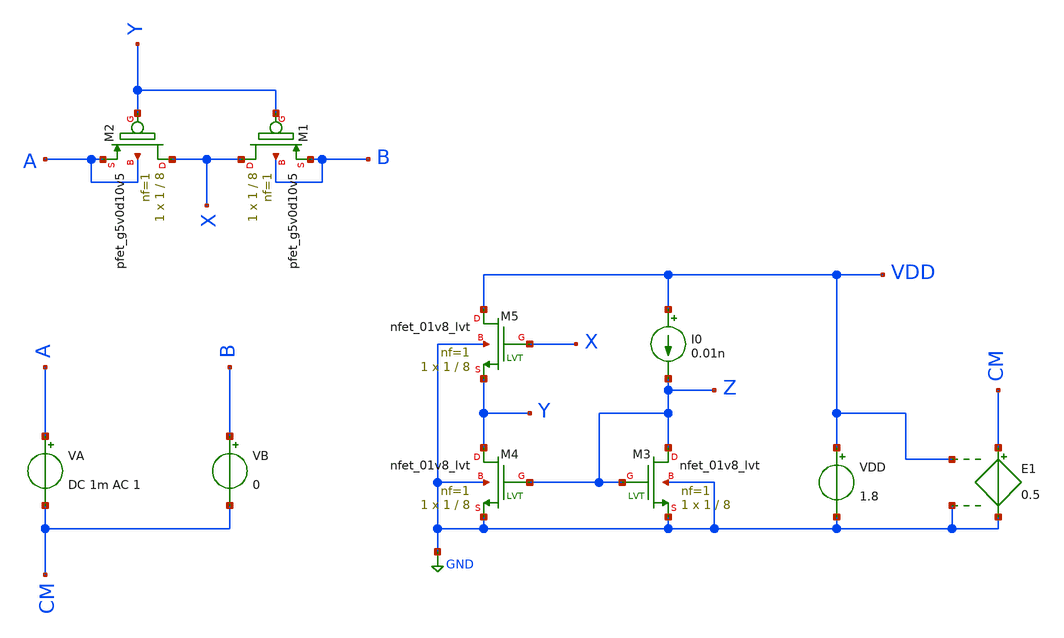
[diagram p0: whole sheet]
** sch_path: xschem/MISC/pseudo/pseudo_tune_tb.sch
* Copyright 2020 Stefan Frederik Schippers
* Licensed under the Apache License, Version 2.0 (the "License");
* you may not use this file except in compliance with the License.
* You may obtain a copy of the License at
* https://www.apache.org/licenses/LICENSE-2.0
* Unless required by applicable law or agreed to in writing, software
* distributed under the License is distributed on an "AS IS" BASIS,
* WITHOUT WARRANTIES OR CONDITIONS OF ANY KIND, either express or implied.
* See the License for the specific language governing permissions and
* limitations under the License.
**.subckt pseudo_tune_tb
XM1 X Y B B sky130_fd_pr__pfet_g5v0d10v5 L=8 W=1 nf=1 ad='int((nf+1)/2) * W/nf * 0.29' as='int((nf+2)/2) * W/nf * 0.29'
+ pd='2*int((nf+1)/2) * (W/nf + 0.29)' ps='2*int((nf+2)/2) * (W/nf + 0.29)' nrd='0.29 / W' nrs='0.29 / W'
+ sa=0 sb=0 sd=0 mult=1 m=1
XM2 X Y A A sky130_fd_pr__pfet_g5v0d10v5 L=8 W=1 nf=1 ad='int((nf+1)/2) * W/nf * 0.29' as='int((nf+2)/2) * W/nf * 0.29'
+ pd='2*int((nf+1)/2) * (W/nf + 0.29)' ps='2*int((nf+2)/2) * (W/nf + 0.29)' nrd='0.29 / W' nrs='0.29 / W'
+ sa=0 sb=0 sd=0 mult=1 m=1
VA A CM DC 1m AC 1
VB B CM 0
I0 VDD Z 0.01n
VDD VDD GND 1.8
E1 CM GND VDD GND 0.5
XM3 Z Z GND GND sky130_fd_pr__nfet_01v8_lvt L=8 W=1 nf=1 ad='int((nf+1)/2) * W/nf * 0.29' as='int((nf+2)/2) * W/nf * 0.29'
+ pd='2*int((nf+1)/2) * (W/nf + 0.29)' ps='2*int((nf+2)/2) * (W/nf + 0.29)' nrd='0.29 / W' nrs='0.29 / W'
+ sa=0 sb=0 sd=0 mult=1 m=1
XM4 Y Z GND GND sky130_fd_pr__nfet_01v8_lvt L=8 W=1 nf=1 ad='int((nf+1)/2) * W/nf * 0.29' as='int((nf+2)/2) * W/nf * 0.29'
+ pd='2*int((nf+1)/2) * (W/nf + 0.29)' ps='2*int((nf+2)/2) * (W/nf + 0.29)' nrd='0.29 / W' nrs='0.29 / W'
+ sa=0 sb=0 sd=0 mult=1 m=1
XM5 VDD X Y GND sky130_fd_pr__nfet_01v8_lvt L=8 W=1 nf=1 ad='int((nf+1)/2) * W/nf * 0.29' as='int((nf+2)/2) * W/nf * 0.29'
+ pd='2*int((nf+1)/2) * (W/nf + 0.29)' ps='2*int((nf+2)/2) * (W/nf + 0.29)' nrd='0.29 / W' nrs='0.29 / W'
+ sa=0 sb=0 sd=0 mult=1 m=1
**** begin user architecture code



.nodeset v(x) = 0.9
.param mc_mm_switch=0

.options gmin=1e-18
*.options rshunt = 1.0e15

.control
  op
  print x y z a b

  ac DEC 1 1 1
  print 1/abs(I(VA))

  dc VA -0.9 0.9 1.1m
  let r=abs(deriv(v(a))/deriv(i(va)))
  plot r ylog

.endc





.include /usr/share/pdk/sky130A/libs.ref/spi/sky130_fd_pr/sky130_fd_pr__pfet_g5v0d10v5__ff.corner.spice
.include /usr/share/pdk/sky130A/libs.ref/spi/sky130_fd_pr/sky130_fd_pr__pfet_g5v0d10v5__mismatch.corner.spice
.include /usr/share/pdk/sky130A/libs.ref/spi/sky130_fd_pr/sky130_fd_pr__nfet_g5v0d10v5__ff.corner.spice
.include /usr/share/pdk/sky130A/libs.ref/spi/sky130_fd_pr/sky130_fd_pr__nfet_g5v0d10v5__mismatch.corner.spice

.include /usr/share/pdk/sky130A/libs.ref/spi/sky130_fd_pr/sky130_fd_pr__nfet_01v8_lvt__tt.corner.spice
.include /usr/share/pdk/sky130A/libs.ref/spi/sky130_fd_pr/sky130_fd_pr__nfet_01v8_lvt__mismatch.corner.spice
.include /usr/share/pdk/sky130A/libs.ref/spi/sky130_fd_pr/sky130_fd_pr__pfet_01v8_lvt__tt.corner.spice
.include /usr/share/pdk/sky130A/libs.ref/spi/sky130_fd_pr/sky130_fd_pr__pfet_01v8_lvt__mismatch.corner.spice

.include ~/OpenPDK/skywater-pdk/skywater-pdk/libraries/sky130_fd_pr/latest/models/all.spice


**** end user architecture code
**.ends
.GLOBAL GND
.end
